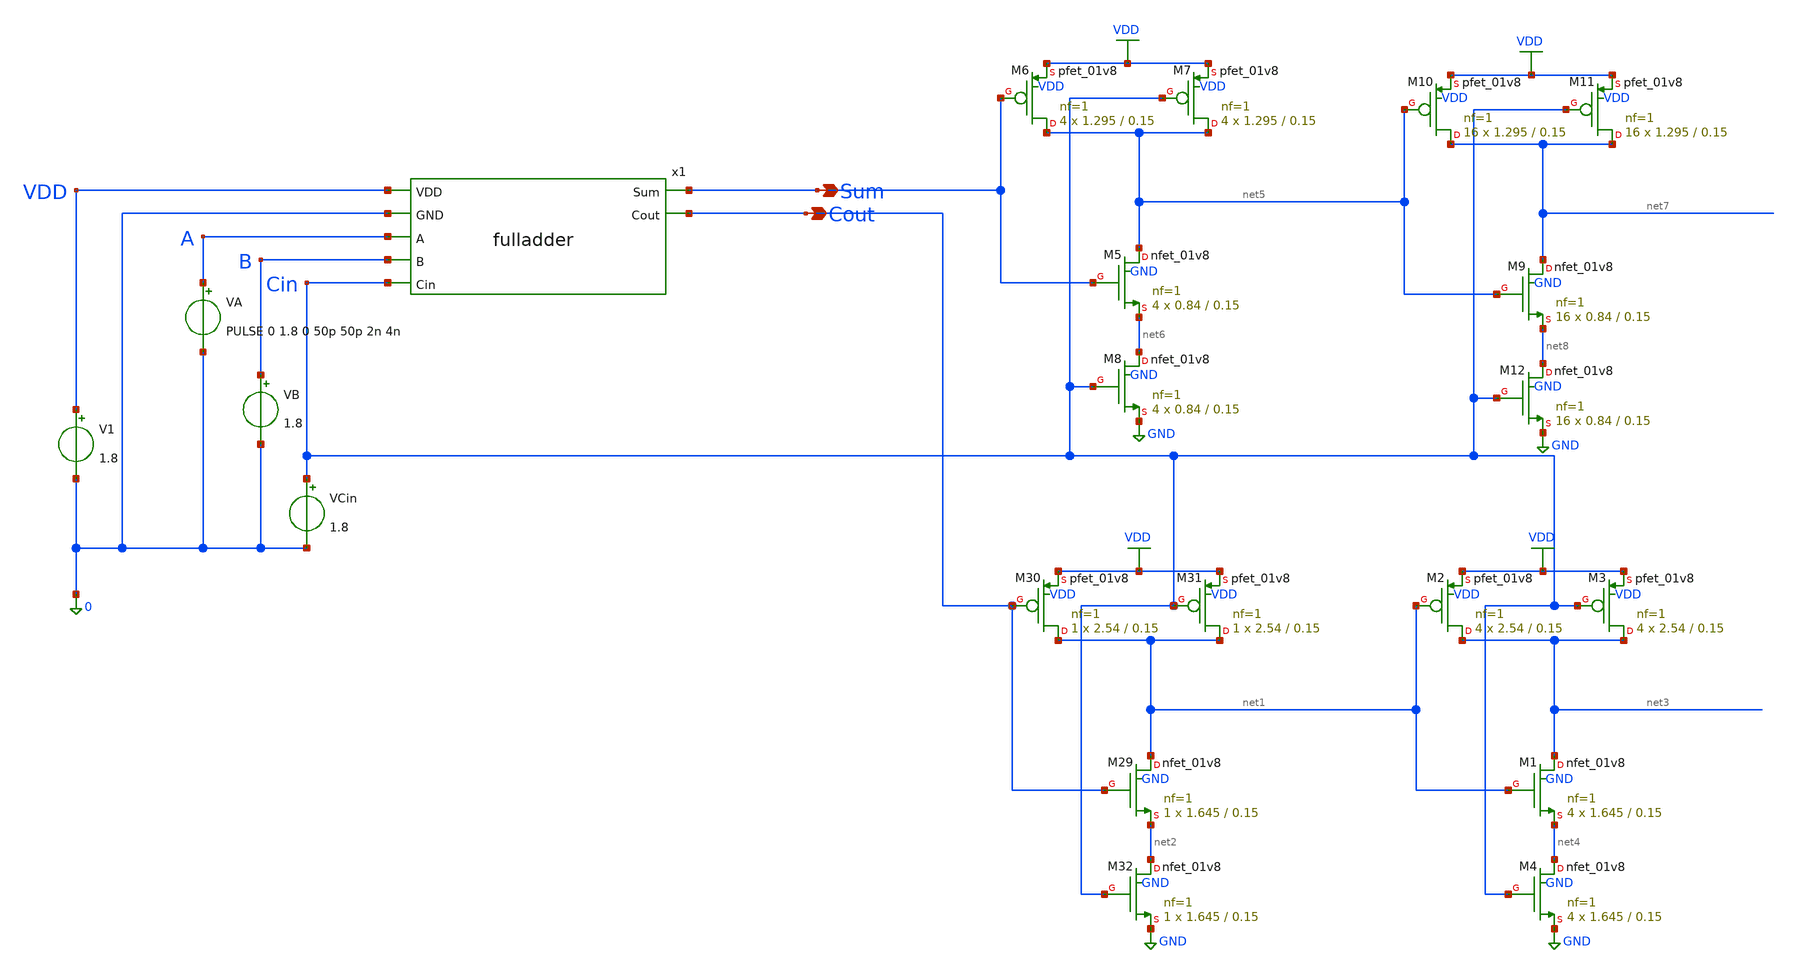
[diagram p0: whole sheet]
** sch_path: testbench/fa_tb_delay.sch
**.subckt fa_tb_delay Cout Sum
*.opin Cout
*.opin Sum
x1 VDD 0 Sum A B Cin Cout fulladder
V1 VDD 0 1.8
VA A 0 PULSE 0 1.8 0 50p 50p 2n 4n
VB B 0 1.8
VCin Cin 0 1.8
XM29 net1 Cout net2 GND sky130_fd_pr__nfet_01v8 L=0.15 W=1.645 nf=1 ad='int((1 + 1)/2) * 1.645 / 1 * 0.29'
+ as='int((1 + 2)/2) * 1.645 / 1 * 0.29' pd='2*int((1 + 1)/2) * (1.645 / 1 + 0.29)' ps='2*int((1 + 2)/2) * (1.645 / 1 + 0.29)'
+ nrd='0.29 / 1.645 ' nrs='0.29 / 1.645 ' sa=0 sb=0 sd=0 mult=1 m=1
XM30 net1 Cout VDD VDD sky130_fd_pr__pfet_01v8 L=0.15 W=2.54 nf=1 ad='int((1 + 1)/2) * 2.54 / 1 * 0.29'
+ as='int((1 + 2)/2) * 2.54 / 1 * 0.29' pd='2*int((1 + 1)/2) * (2.54 / 1 + 0.29)' ps='2*int((1 + 2)/2) * (2.54 / 1 + 0.29)'
+ nrd='0.29 / 2.54 ' nrs='0.29 / 2.54 ' sa=0 sb=0 sd=0 mult=1 m=1
XM31 net1 Cin VDD VDD sky130_fd_pr__pfet_01v8 L=0.15 W=2.54 nf=1 ad='int((1 + 1)/2) * 2.54 / 1 * 0.29'
+ as='int((1 + 2)/2) * 2.54 / 1 * 0.29' pd='2*int((1 + 1)/2) * (2.54 / 1 + 0.29)' ps='2*int((1 + 2)/2) * (2.54 / 1 + 0.29)'
+ nrd='0.29 / 2.54 ' nrs='0.29 / 2.54 ' sa=0 sb=0 sd=0 mult=1 m=1
XM32 net2 Cin GND GND sky130_fd_pr__nfet_01v8 L=0.15 W=1.645 nf=1 ad='int((1 + 1)/2) * 1.645 / 1 * 0.29'
+ as='int((1 + 2)/2) * 1.645 / 1 * 0.29' pd='2*int((1 + 1)/2) * (1.645 / 1 + 0.29)' ps='2*int((1 + 2)/2) * (1.645 / 1 + 0.29)'
+ nrd='0.29 / 1.645 ' nrs='0.29 / 1.645 ' sa=0 sb=0 sd=0 mult=1 m=1
XM1 net3 net1 net4 GND sky130_fd_pr__nfet_01v8 L=0.15 W=1.645 nf=1 ad='int((1 + 1)/2) * 1.645 / 1 * 0.29'
+ as='int((1 + 2)/2) * 1.645 / 1 * 0.29' pd='2*int((1 + 1)/2) * (1.645 / 1 + 0.29)' ps='2*int((1 + 2)/2) * (1.645 / 1 + 0.29)'
+ nrd='0.29 / 1.645 ' nrs='0.29 / 1.645 ' sa=0 sb=0 sd=0 mult=4 m=4
XM2 net3 net1 VDD VDD sky130_fd_pr__pfet_01v8 L=0.15 W=2.54 nf=1 ad='int((1 + 1)/2) * 2.54 / 1 * 0.29'
+ as='int((1 + 2)/2) * 2.54 / 1 * 0.29' pd='2*int((1 + 1)/2) * (2.54 / 1 + 0.29)' ps='2*int((1 + 2)/2) * (2.54 / 1 + 0.29)'
+ nrd='0.29 / 2.54 ' nrs='0.29 / 2.54 ' sa=0 sb=0 sd=0 mult=4 m=4
XM3 net3 Cin VDD VDD sky130_fd_pr__pfet_01v8 L=0.15 W=2.54 nf=1 ad='int((1 + 1)/2) * 2.54 / 1 * 0.29'
+ as='int((1 + 2)/2) * 2.54 / 1 * 0.29' pd='2*int((1 + 1)/2) * (2.54 / 1 + 0.29)' ps='2*int((1 + 2)/2) * (2.54 / 1 + 0.29)'
+ nrd='0.29 / 2.54 ' nrs='0.29 / 2.54 ' sa=0 sb=0 sd=0 mult=4 m=4
XM4 net4 Cin GND GND sky130_fd_pr__nfet_01v8 L=0.15 W=1.645 nf=1 ad='int((1 + 1)/2) * 1.645 / 1 * 0.29'
+ as='int((1 + 2)/2) * 1.645 / 1 * 0.29' pd='2*int((1 + 1)/2) * (1.645 / 1 + 0.29)' ps='2*int((1 + 2)/2) * (1.645 / 1 + 0.29)'
+ nrd='0.29 / 1.645 ' nrs='0.29 / 1.645 ' sa=0 sb=0 sd=0 mult=4 m=4
XM5 net5 Sum net6 GND sky130_fd_pr__nfet_01v8 L=0.15 W=0.84 nf=1 ad='int((1 + 1)/2) * 0.84 / 1 * 0.29'
+ as='int((1 + 2)/2) * 0.84 / 1 * 0.29' pd='2*int((1 + 1)/2) * (0.84 / 1 + 0.29)' ps='2*int((1 + 2)/2) * (0.84 / 1 + 0.29)'
+ nrd='0.29 / 0.84 ' nrs='0.29 / 0.84 ' sa=0 sb=0 sd=0 mult=4 m=4
XM6 net5 Sum VDD VDD sky130_fd_pr__pfet_01v8 L=0.15 W=1.295 nf=1 ad='int((1 + 1)/2) * 1.295 / 1 * 0.29'
+ as='int((1 + 2)/2) * 1.295 / 1 * 0.29' pd='2*int((1 + 1)/2) * (1.295 / 1 + 0.29)' ps='2*int((1 + 2)/2) * (1.295 / 1 + 0.29)'
+ nrd='0.29 / 1.295 ' nrs='0.29 / 1.295 ' sa=0 sb=0 sd=0 mult=4 m=4
XM7 net5 Cin VDD VDD sky130_fd_pr__pfet_01v8 L=0.15 W=1.295 nf=1 ad='int((1 + 1)/2) * 1.295 / 1 * 0.29'
+ as='int((1 + 2)/2) * 1.295 / 1 * 0.29' pd='2*int((1 + 1)/2) * (1.295 / 1 + 0.29)' ps='2*int((1 + 2)/2) * (1.295 / 1 + 0.29)'
+ nrd='0.29 / 1.295 ' nrs='0.29 / 1.295 ' sa=0 sb=0 sd=0 mult=4 m=4
XM8 net6 Cin GND GND sky130_fd_pr__nfet_01v8 L=0.15 W=0.84 nf=1 ad='int((1 + 1)/2) * 0.84 / 1 * 0.29'
+ as='int((1 + 2)/2) * 0.84 / 1 * 0.29' pd='2*int((1 + 1)/2) * (0.84 / 1 + 0.29)' ps='2*int((1 + 2)/2) * (0.84 / 1 + 0.29)'
+ nrd='0.29 / 0.84 ' nrs='0.29 / 0.84 ' sa=0 sb=0 sd=0 mult=4 m=4
XM9 net7 net5 net8 GND sky130_fd_pr__nfet_01v8 L=0.15 W=0.84 nf=1 ad='int((1 + 1)/2) * 0.84 / 1 * 0.29'
+ as='int((1 + 2)/2) * 0.84 / 1 * 0.29' pd='2*int((1 + 1)/2) * (0.84 / 1 + 0.29)' ps='2*int((1 + 2)/2) * (0.84 / 1 + 0.29)'
+ nrd='0.29 / 0.84 ' nrs='0.29 / 0.84 ' sa=0 sb=0 sd=0 mult=16 m=16
XM10 net7 net5 VDD VDD sky130_fd_pr__pfet_01v8 L=0.15 W=1.295 nf=1 ad='int((1 + 1)/2) * 1.295 / 1 * 0.29'
+ as='int((1 + 2)/2) * 1.295 / 1 * 0.29' pd='2*int((1 + 1)/2) * (1.295 / 1 + 0.29)' ps='2*int((1 + 2)/2) * (1.295 / 1 + 0.29)'
+ nrd='0.29 / 1.295 ' nrs='0.29 / 1.295 ' sa=0 sb=0 sd=0 mult=16 m=16
XM11 net7 Cin VDD VDD sky130_fd_pr__pfet_01v8 L=0.15 W=1.295 nf=1 ad='int((1 + 1)/2) * 1.295 / 1 * 0.29'
+ as='int((1 + 2)/2) * 1.295 / 1 * 0.29' pd='2*int((1 + 1)/2) * (1.295 / 1 + 0.29)' ps='2*int((1 + 2)/2) * (1.295 / 1 + 0.29)'
+ nrd='0.29 / 1.295 ' nrs='0.29 / 1.295 ' sa=0 sb=0 sd=0 mult=16 m=16
XM12 net8 Cin GND GND sky130_fd_pr__nfet_01v8 L=0.15 W=0.84 nf=1 ad='int((1 + 1)/2) * 0.84 / 1 * 0.29'
+ as='int((1 + 2)/2) * 0.84 / 1 * 0.29' pd='2*int((1 + 1)/2) * (0.84 / 1 + 0.29)' ps='2*int((1 + 2)/2) * (0.84 / 1 + 0.29)'
+ nrd='0.29 / 0.84 ' nrs='0.29 / 0.84 ' sa=0 sb=0 sd=0 mult=16 m=16
**** begin user architecture code


.lib /usr/local/share/pdk/sky130A/libs.tech/ngspice/sky130.lib.spice tt
.include /home/dat02/projects/cmos-full-adder-sky130/layout/fulladder_pex.spice
.control
	tran 0.1p 10n
	meas tran tpdr trig v(a) val=0.9 rise=1 targ v(sum) val=0.9 rise=1
	meas tran tpdf trig v(a) val=0.9 fall=1 targ v(sum) val=0.9 fall=1
	let tpd = (tpdr + tpdf) / 2
	print tpd
.endc


**** end user architecture code
**.ends
.GLOBAL GND
.GLOBAL VDD
.end
